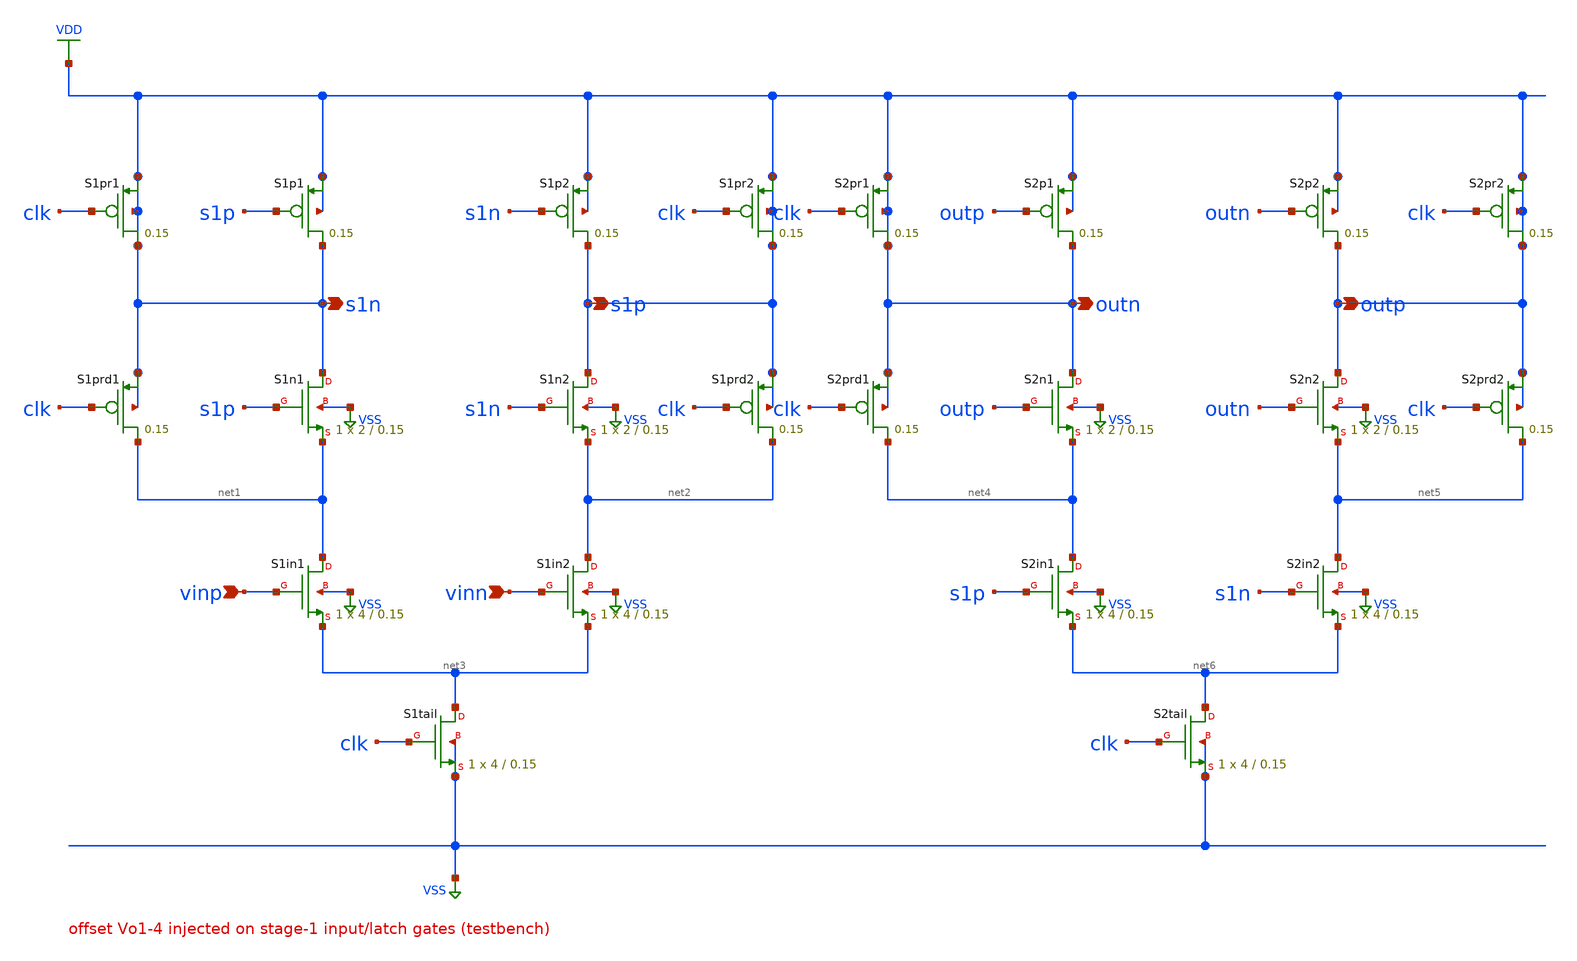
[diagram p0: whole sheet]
** sch_path: eda/hero/schematics/dsa.sch
**.subckt dsa vinp vinn s1n s1p outn outp
*.ipin vinp
*.ipin vinn
*.opin s1n
*.opin s1p
*.opin outn
*.opin outp
XS1p1 s1n s1p s1n s1n sky130_fd_pr__sky130_fd_pr__pfet_01v8 L=0.15 W=2 nrd='0.29 / W' nrs='0.29 / W'
+ sa=0 sb=0 sd=0 mult=1 m=1
XS1p2 s1n s1n s1n s1n sky130_fd_pr__sky130_fd_pr__pfet_01v8 L=0.15 W=2 nrd='0.29 / W' nrs='0.29 / W'
+ sa=0 sb=0 sd=0 mult=1 m=1
XS1pr1 s1n clk s1n s1n sky130_fd_pr__sky130_fd_pr__pfet_01v8 L=0.15 W=2 nrd='0.29 / W' nrs='0.29 / W'
+ sa=0 sb=0 sd=0 mult=1 m=1
XS1pr2 s1n clk s1n s1n sky130_fd_pr__sky130_fd_pr__pfet_01v8 L=0.15 W=2 nrd='0.29 / W' nrs='0.29 / W'
+ sa=0 sb=0 sd=0 mult=1 m=1
XS1n1 s1n s1p net1 VSS sky130_fd_pr__sky130_fd_pr__nfet_01v8 L=0.15 W=2 nrd='0.29 / W' nrs='0.29 / W'
+ sa=0 sb=0 sd=0 mult=1 m=1
XS1n2 s1n s1n net2 VSS sky130_fd_pr__sky130_fd_pr__nfet_01v8 L=0.15 W=2 nrd='0.29 / W' nrs='0.29 / W'
+ sa=0 sb=0 sd=0 mult=1 m=1
XS1prd1 net1 clk s1n s1n sky130_fd_pr__sky130_fd_pr__pfet_01v8 L=0.15 W=2 nrd='0.29 / W' nrs='0.29 / W'
+ sa=0 sb=0 sd=0 mult=1 m=1
XS1prd2 net2 clk s1n s1n sky130_fd_pr__sky130_fd_pr__pfet_01v8 L=0.15 W=2 nrd='0.29 / W' nrs='0.29 / W'
+ sa=0 sb=0 sd=0 mult=1 m=1
XS1in1 net1 vinp net3 VSS sky130_fd_pr__sky130_fd_pr__nfet_01v8 L=0.15 W=4 nrd='0.29 / W' nrs='0.29 / W'
+ sa=0 sb=0 sd=0 mult=1 m=1
XS1in2 net2 vinn net3 VSS sky130_fd_pr__sky130_fd_pr__nfet_01v8 L=0.15 W=4 nrd='0.29 / W' nrs='0.29 / W'
+ sa=0 sb=0 sd=0 mult=1 m=1
XS1tail net3 clk VSS VSS sky130_fd_pr__sky130_fd_pr__nfet_01v8 L=0.15 W=4 nrd='0.29 / W' nrs='0.29 / W'
+ sa=0 sb=0 sd=0 mult=1 m=1
XS2p1 s1n outp s1n s1n sky130_fd_pr__sky130_fd_pr__pfet_01v8 L=0.15 W=2 nrd='0.29 / W' nrs='0.29 / W'
+ sa=0 sb=0 sd=0 mult=1 m=1
XS2p2 s1n outn s1n s1n sky130_fd_pr__sky130_fd_pr__pfet_01v8 L=0.15 W=2 nrd='0.29 / W' nrs='0.29 / W'
+ sa=0 sb=0 sd=0 mult=1 m=1
XS2pr1 s1n clk s1n s1n sky130_fd_pr__sky130_fd_pr__pfet_01v8 L=0.15 W=2 nrd='0.29 / W' nrs='0.29 / W'
+ sa=0 sb=0 sd=0 mult=1 m=1
XS2pr2 s1n clk s1n s1n sky130_fd_pr__sky130_fd_pr__pfet_01v8 L=0.15 W=2 nrd='0.29 / W' nrs='0.29 / W'
+ sa=0 sb=0 sd=0 mult=1 m=1
XS2n1 s1n outp net4 VSS sky130_fd_pr__sky130_fd_pr__nfet_01v8 L=0.15 W=2 nrd='0.29 / W' nrs='0.29 / W'
+ sa=0 sb=0 sd=0 mult=1 m=1
XS2n2 s1n outn net5 VSS sky130_fd_pr__sky130_fd_pr__nfet_01v8 L=0.15 W=2 nrd='0.29 / W' nrs='0.29 / W'
+ sa=0 sb=0 sd=0 mult=1 m=1
XS2prd1 net4 clk s1n s1n sky130_fd_pr__sky130_fd_pr__pfet_01v8 L=0.15 W=2 nrd='0.29 / W' nrs='0.29 / W'
+ sa=0 sb=0 sd=0 mult=1 m=1
XS2prd2 net5 clk s1n s1n sky130_fd_pr__sky130_fd_pr__pfet_01v8 L=0.15 W=2 nrd='0.29 / W' nrs='0.29 / W'
+ sa=0 sb=0 sd=0 mult=1 m=1
XS2in1 net4 s1p net6 VSS sky130_fd_pr__sky130_fd_pr__nfet_01v8 L=0.15 W=4 nrd='0.29 / W' nrs='0.29 / W'
+ sa=0 sb=0 sd=0 mult=1 m=1
XS2in2 net5 s1n net6 VSS sky130_fd_pr__sky130_fd_pr__nfet_01v8 L=0.15 W=4 nrd='0.29 / W' nrs='0.29 / W'
+ sa=0 sb=0 sd=0 mult=1 m=1
XS2tail net6 clk VSS VSS sky130_fd_pr__sky130_fd_pr__nfet_01v8 L=0.15 W=4 nrd='0.29 / W' nrs='0.29 / W'
+ sa=0 sb=0 sd=0 mult=1 m=1
**.ends
.GLOBAL VSS
.GLOBAL VDD
.end
